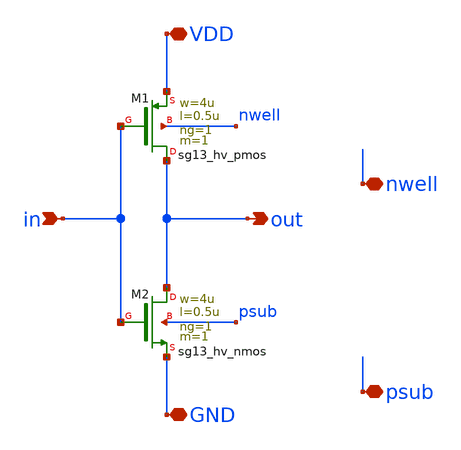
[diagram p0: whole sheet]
** sch_path: xschem/inv.sch
**.subckt inv in GND out VDD nwell psub
*.ipin in
*.iopin GND
*.opin out
*.iopin VDD
*.iopin nwell
*.iopin psub
XM1 out in VDD nwell sg13_hv_pmos w=4u l=0.5u ng=1 m=1 mm_ok=1
XM2 out in GND psub sg13_hv_nmos w=4u l=0.5u ng=1 m=1 mm_ok=1
**.ends
.end
